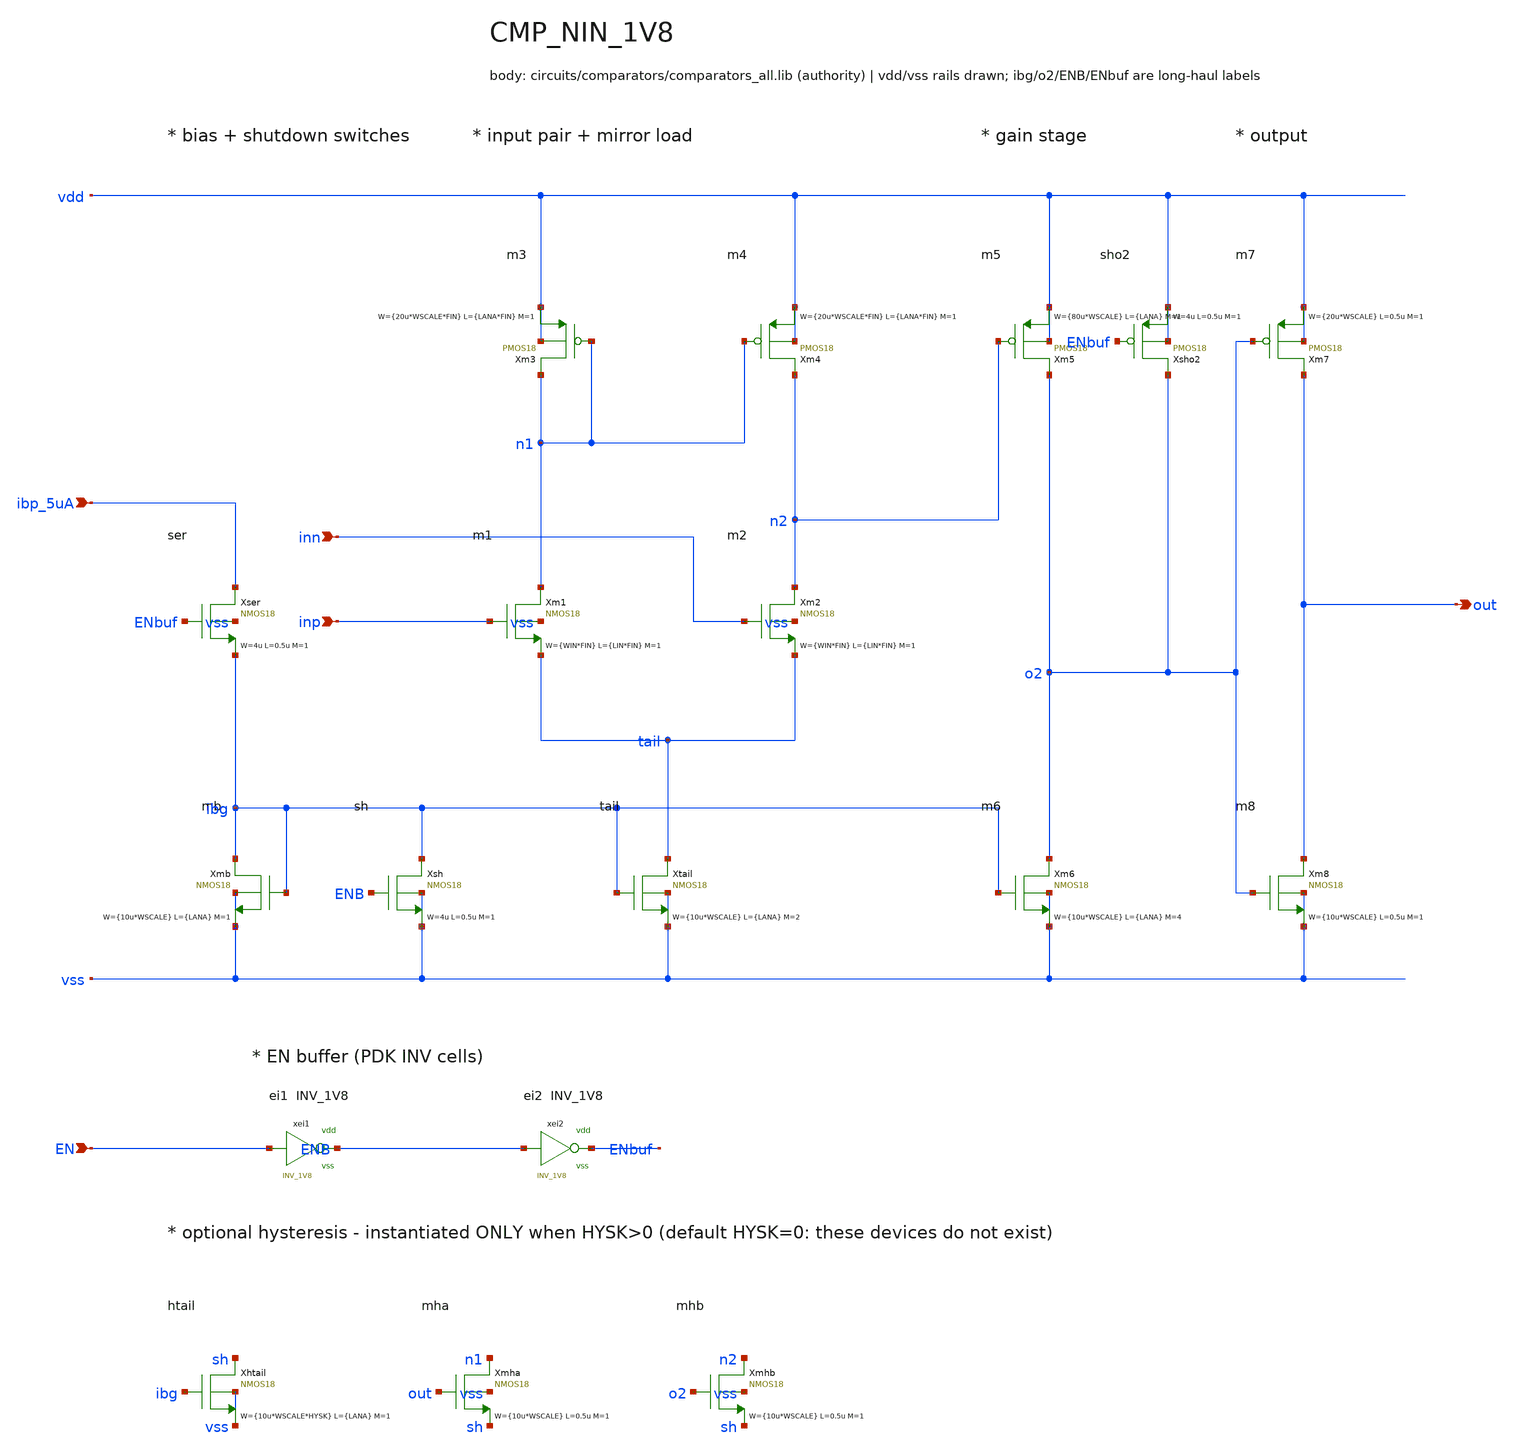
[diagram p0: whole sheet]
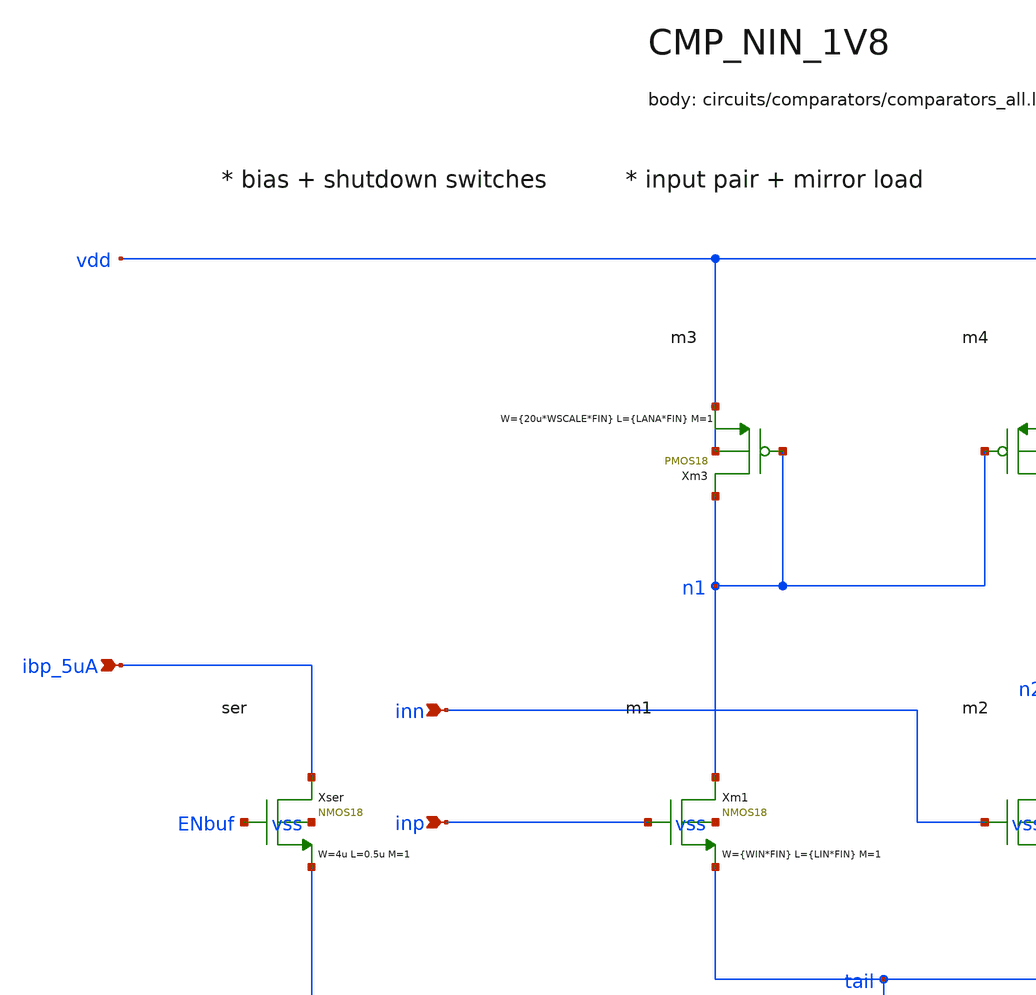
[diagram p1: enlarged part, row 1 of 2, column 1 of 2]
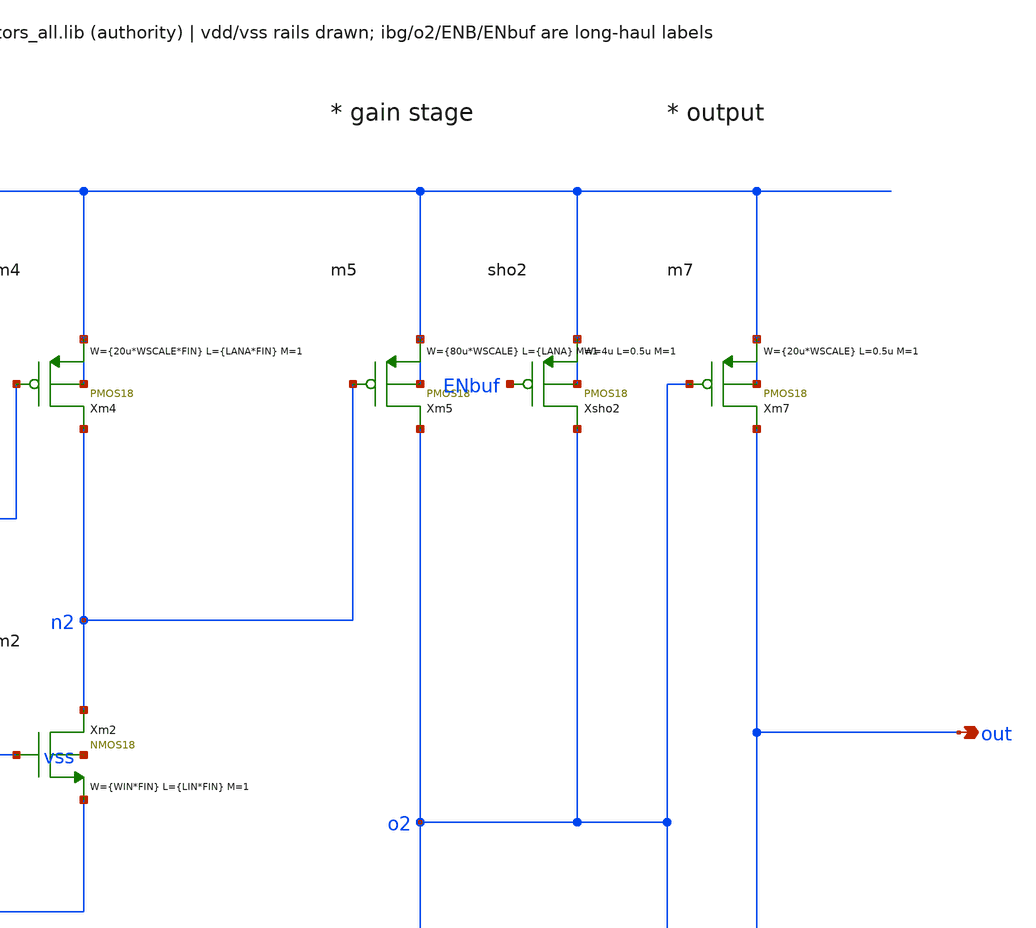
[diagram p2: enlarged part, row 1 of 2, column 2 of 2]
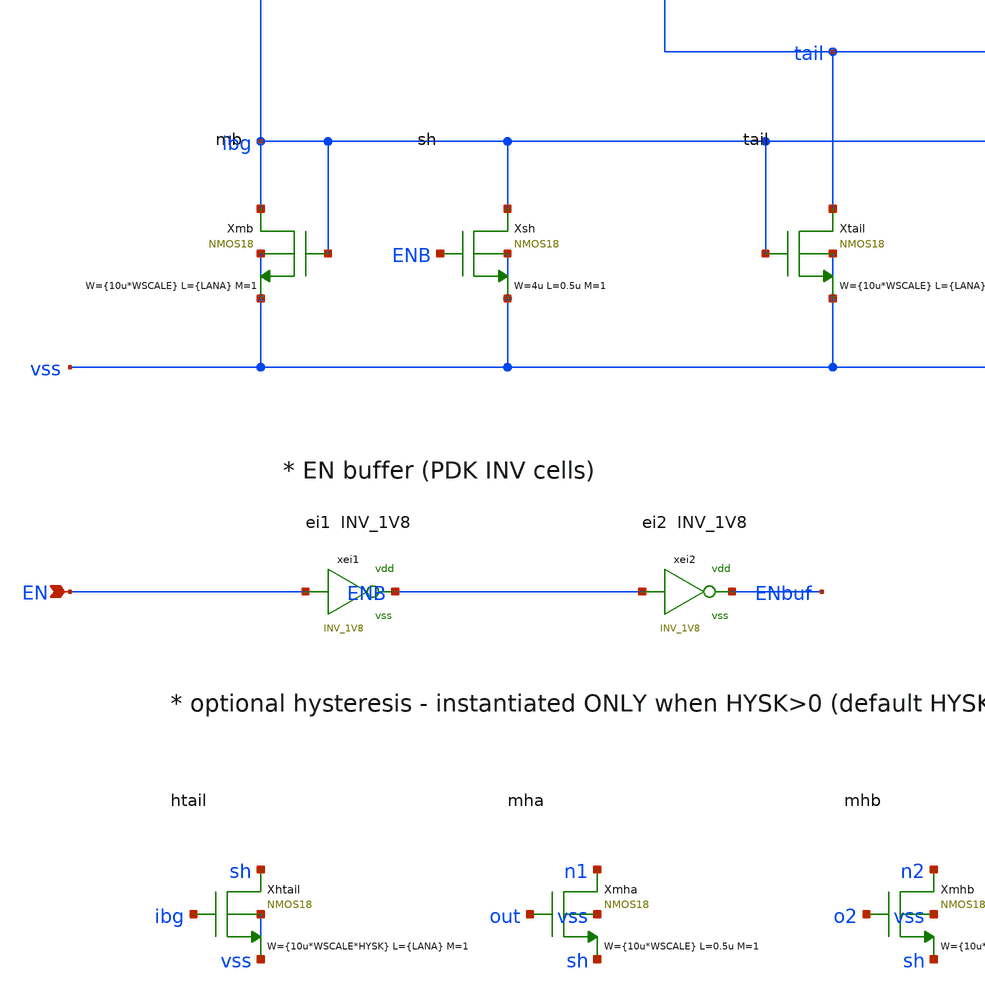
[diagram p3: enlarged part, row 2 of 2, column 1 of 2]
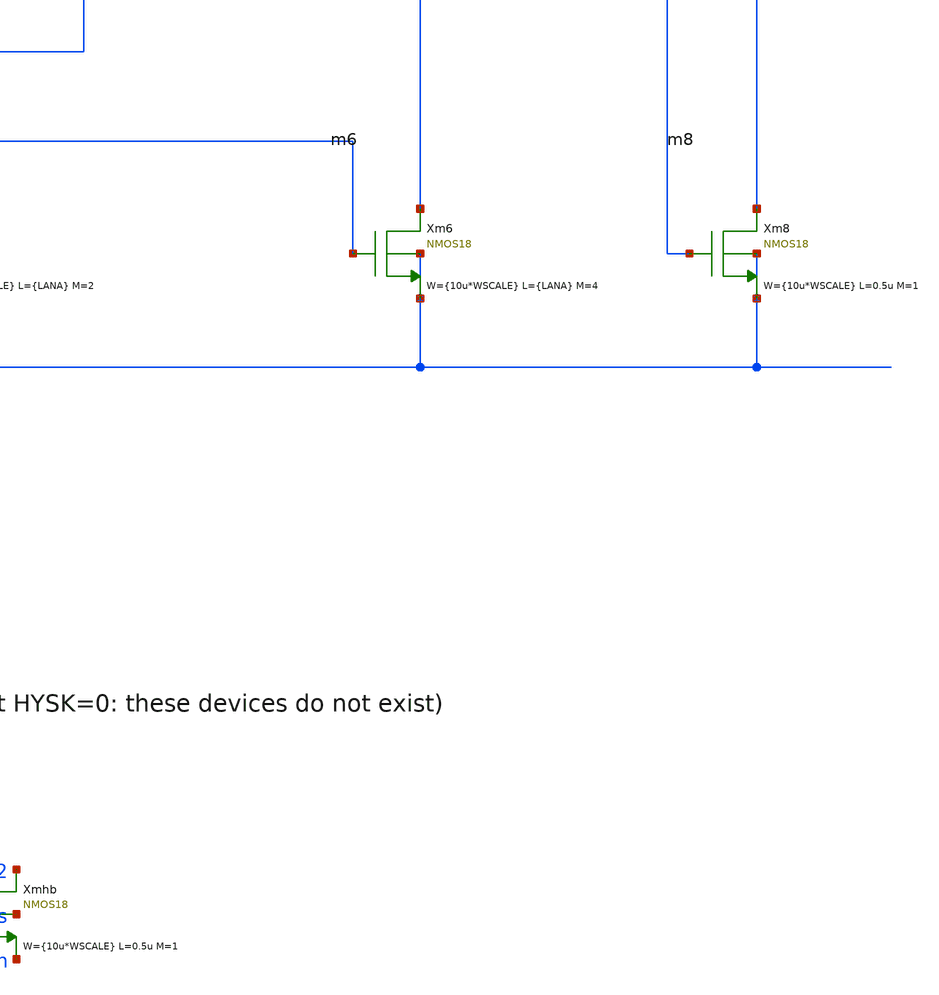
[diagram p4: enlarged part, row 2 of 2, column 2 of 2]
** sch_path: xschem/comparators/CMP_NIN_1V8.sch
**.subckt CMP_NIN_1V8 ibp_5uA out inp inn EN
*.ipin ibp_5uA
*.opin out
*.ipin inp
*.ipin inn
*.ipin EN
Xmb ibg ibg vss vss NMOS18 W={10u*WSCALE} L={LANA} M=1 MM_SIGMA=0
Xtail tail ibg vss vss NMOS18 W={10u*WSCALE} L={LANA} M=2 MM_SIGMA=0
Xm1 n1 inp tail vss NMOS18 W={WIN*FIN} L={LIN*FIN} M=1 MM_SIGMA=0
Xm2 n2 inn tail vss NMOS18 W={WIN*FIN} L={LIN*FIN} M=1 MM_SIGMA=0
Xm3 n1 n1 vdd vdd PMOS18 W={20u*WSCALE*FIN} L={LANA*FIN} M=1 MM_SIGMA=0
Xm4 n2 n1 vdd vdd PMOS18 W={20u*WSCALE*FIN} L={LANA*FIN} M=1 MM_SIGMA=0
Xm5 o2 n2 vdd vdd PMOS18 W={80u*WSCALE} L={LANA} M=1 MM_SIGMA=0
Xm6 o2 ibg vss vss NMOS18 W={10u*WSCALE} L={LANA} M=4 MM_SIGMA=0
Xm7 out o2 vdd vdd PMOS18 W={20u*WSCALE} L=0.5u M=1 MM_SIGMA=0
Xm8 out o2 vss vss NMOS18 W={10u*WSCALE} L=0.5u M=1 MM_SIGMA=0
xei1 EN ENB vdd vss INV_1V8
xei2 ENB ENbuf vdd vss INV_1V8
Xsh ibg ENB vss vss NMOS18 W=4u L=0.5u M=1 MM_SIGMA=0
Xsho2 o2 ENbuf vdd vdd PMOS18 W=4u L=0.5u M=1 MM_SIGMA=0
Xser ibp_5uA ENbuf ibg vss NMOS18 W=4u L=0.5u M=1 MM_SIGMA=0
Xhtail sh ibg vss vss NMOS18 W={10u*WSCALE*HYSK} L={LANA} M=1 MM_SIGMA=0
Xmha n1 out sh vss NMOS18 W={10u*WSCALE} L=0.5u M=1 MM_SIGMA=0
Xmhb n2 o2 sh vss NMOS18 W={10u*WSCALE} L=0.5u M=1 MM_SIGMA=0
**.ends
.end
